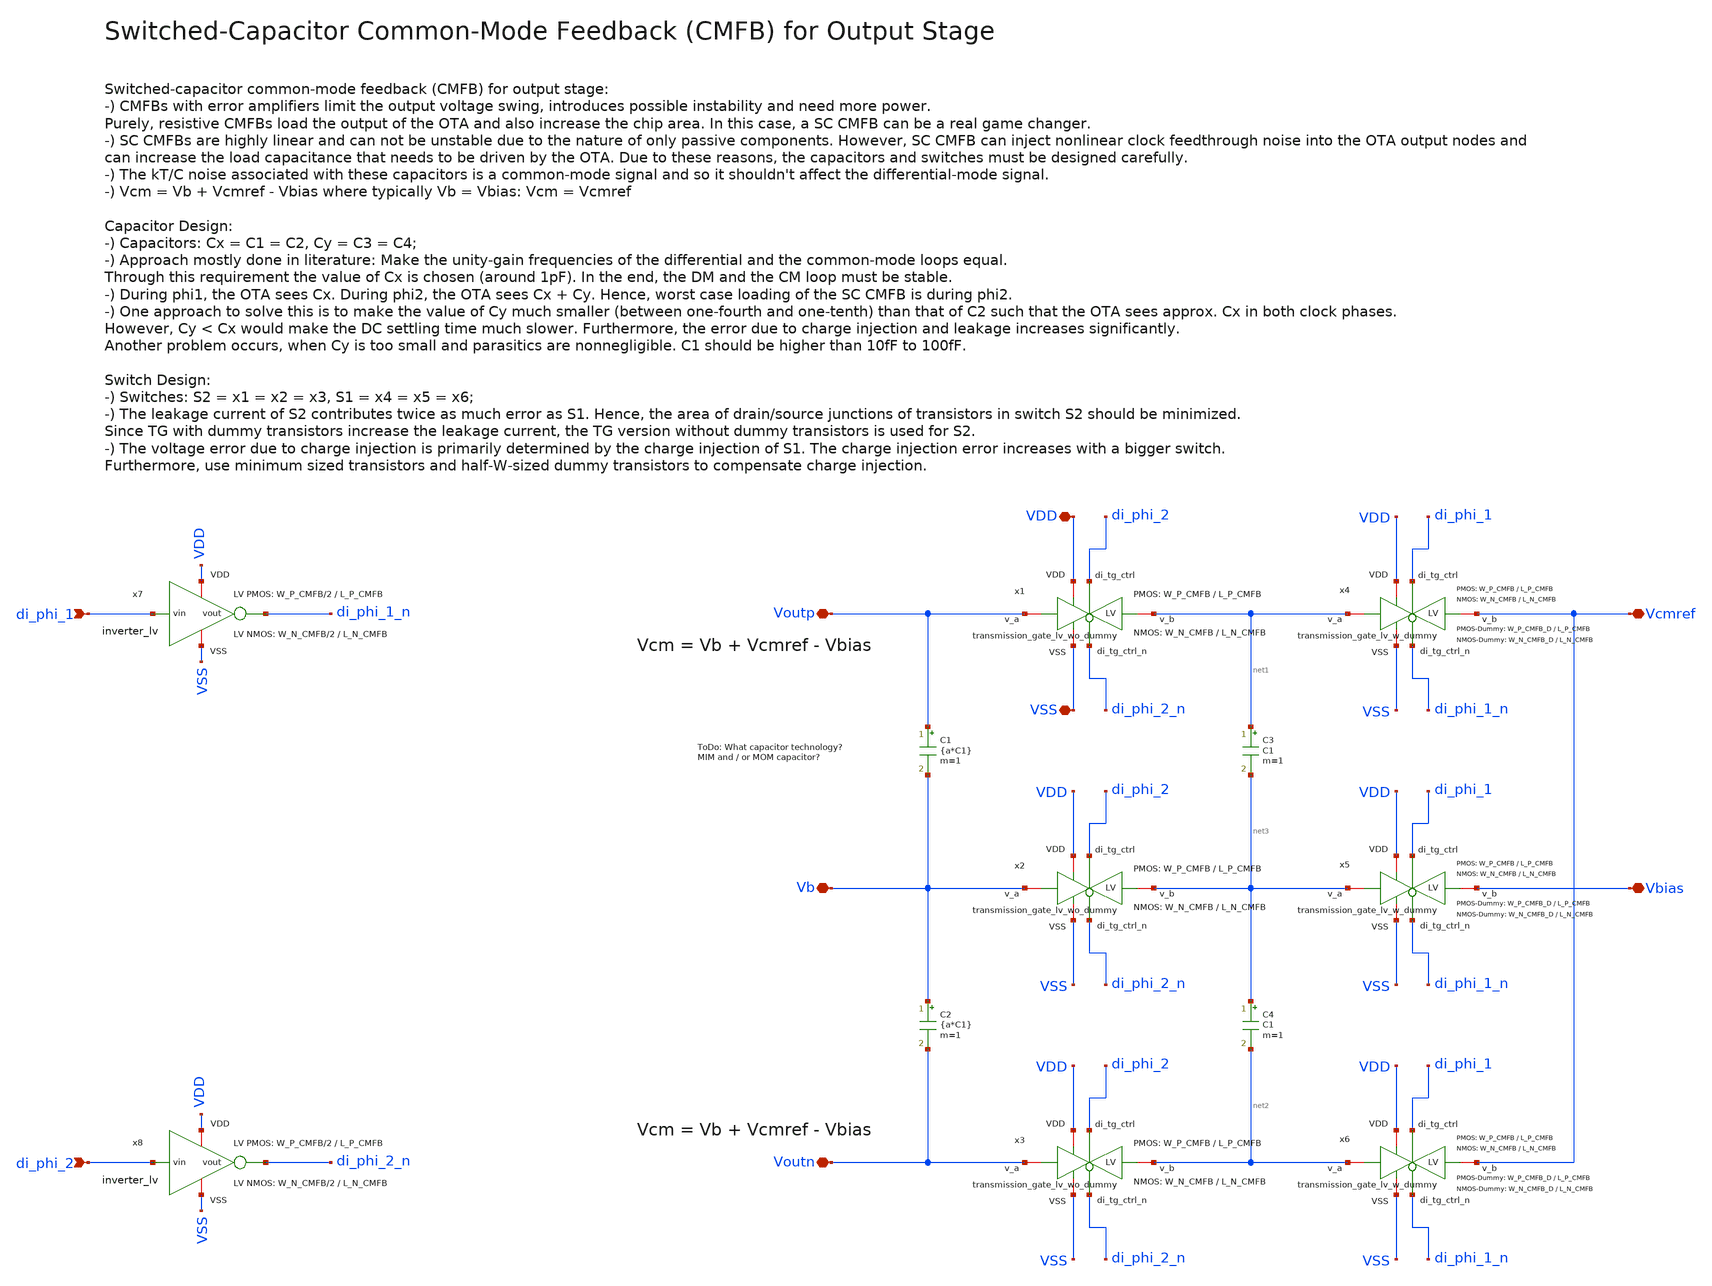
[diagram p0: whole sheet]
** sch_path: SG13G2_ATBS-ADC-main/xschem/bio_amplifier/amplifier_core/sc_cmfb/sc_cmfb_output.sch
**.subckt sc_cmfb_output VSS VDD Vb Voutp Voutn Vbias Vcmref di_phi_1 di_phi_2
*.iopin VSS
*.iopin VDD
*.iopin Vb
*.iopin Voutp
*.iopin Voutn
*.iopin Vbias
*.iopin Vcmref
*.ipin di_phi_1
*.ipin di_phi_2
x1 VDD di_phi_2 VSS net1 Voutp di_phi_2_n transmission_gate_lv_wo_dummy W_P=W_P_CMFB L_P=L_P_CMFB
+ W_N=W_N_CMFB L_N=L_N_CMFB
C1 Voutp Vb {a*C1} m=1
x2 VDD di_phi_2 VSS net3 Vb di_phi_2_n transmission_gate_lv_wo_dummy W_P=W_P_CMFB L_P=L_P_CMFB
+ W_N=W_N_CMFB L_N=L_N_CMFB
x3 VDD di_phi_2 VSS net2 Voutn di_phi_2_n transmission_gate_lv_wo_dummy W_P=W_P_CMFB L_P=L_P_CMFB
+ W_N=W_N_CMFB L_N=L_N_CMFB
C2 Vb Voutn {a*C1} m=1
C3 net1 net3 C1 m=1
C4 net3 net2 C1 m=1
x7 VDD di_phi_1 di_phi_1_n VSS inverter_lv W_P=W_P_CMFB/2 L_P=L_P_CMFB W_N=W_N_CMFB/2 L_N=L_N_CMFB
x8 VDD di_phi_2 di_phi_2_n VSS inverter_lv W_P=W_P_CMFB/2 L_P=L_P_CMFB W_N=W_N_CMFB/2 L_N=L_N_CMFB
x4 VDD di_phi_1 VSS Vcmref net1 di_phi_1_n transmission_gate_lv_w_dummy W_P=W_P_CMFB L_P=L_P_CMFB
+ W_N=W_N_CMFB L_N=L_N_CMFB W_P_D=W_P_CMFB_D L_P_D=L_P_CMFB W_N_D=W_N_CMFB_D L_N_D=L_N_CMFB
x5 VDD di_phi_1 VSS Vbias net3 di_phi_1_n transmission_gate_lv_w_dummy W_P=W_P_CMFB L_P=L_P_CMFB
+ W_N=W_N_CMFB L_N=L_N_CMFB W_P_D=W_P_CMFB_D L_P_D=L_P_CMFB W_N_D=W_N_CMFB_D L_N_D=L_N_CMFB
x6 VDD di_phi_1 VSS Vcmref net2 di_phi_1_n transmission_gate_lv_w_dummy W_P=W_P_CMFB L_P=L_P_CMFB
+ W_N=W_N_CMFB L_N=L_N_CMFB W_P_D=W_P_CMFB_D L_P_D=L_P_CMFB W_N_D=W_N_CMFB_D L_N_D=L_N_CMFB
**.ends

* expanding   symbol:  transmission_gate/transmission_gate_lv_wo_dummy.sym # of pins=6
** sym_path: SG13G2_ATBS-ADC-main/xschem/transmission_gate/transmission_gate_lv_wo_dummy.sym
** sch_path: SG13G2_ATBS-ADC-main/xschem/transmission_gate/transmission_gate_lv_wo_dummy.sch
.subckt transmission_gate_lv_wo_dummy VDD di_tg_ctrl VSS v_b v_a di_tg_ctrl_n  W_P=1.0u L_P=0.13u
+ W_N=1.0u L_N=0.13u
*.iopin v_a
*.iopin v_b
*.iopin VDD
*.iopin VSS
*.ipin di_tg_ctrl
*.ipin di_tg_ctrl_n
XM1 v_a di_tg_ctrl v_b VSS sg13_lv_nmos w=W_N l=L_N ng=1 m=1 mm_ok=1
XM2 v_a di_tg_ctrl_n v_b VDD sg13_lv_pmos w=W_P l=L_P ng=1 m=1 mm_ok=1
.ends


* expanding   symbol:  inverter/inverter_lv.sym # of pins=4
** sym_path: SG13G2_ATBS-ADC-main/xschem/inverter/inverter_lv.sym
** sch_path: SG13G2_ATBS-ADC-main/xschem/inverter/inverter_lv.sch
.subckt inverter_lv VDD vin vout VSS  W_P=3.0u L_P=0.13u W_N=1.0u L_N=0.13u
*.ipin vin
*.iopin VDD
*.iopin VSS
*.opin vout
XM1 vout vin VDD VDD sg13_lv_pmos w=W_P l=L_P ng=1 m=1 mm_ok=1
XM2 vout vin VSS VSS sg13_lv_nmos w=W_N l=L_N ng=1 m=1 mm_ok=1
.ends


* expanding   symbol:  transmission_gate/transmission_gate_lv_w_dummy.sym # of pins=6
** sym_path: SG13G2_ATBS-ADC-main/xschem/transmission_gate/transmission_gate_lv_w_dummy.sym
** sch_path: SG13G2_ATBS-ADC-main/xschem/transmission_gate/transmission_gate_lv_w_dummy.sch
.subckt transmission_gate_lv_w_dummy VDD di_tg_ctrl VSS v_b v_a di_tg_ctrl_n  W_P=2.0u L_P=0.13u
+ W_N=2.0u L_N=0.13u W_P_D=1.0u L_P_D=0.13u W_N_D=1.0u L_N_D=0.13u
*.iopin v_a
*.iopin v_b
*.iopin VDD
*.iopin VSS
*.ipin di_tg_ctrl
*.ipin di_tg_ctrl_n
XM1 v_a di_tg_ctrl v_b VSS sg13_lv_nmos w=W_N l=L_N ng=1 m=1 mm_ok=1
XM2 v_a di_tg_ctrl_n v_b VDD sg13_lv_pmos w=W_P l=L_P ng=1 m=1 mm_ok=1
XMdummy2 v_b di_tg_ctrl v_b VDD sg13_lv_pmos w=W_P_D l=L_P_D ng=1 m=1 mm_ok=1
XMdummy1 v_b di_tg_ctrl_n v_b VSS sg13_lv_nmos w=W_N_D l=L_N_D ng=1 m=1 mm_ok=1
.ends

.end
